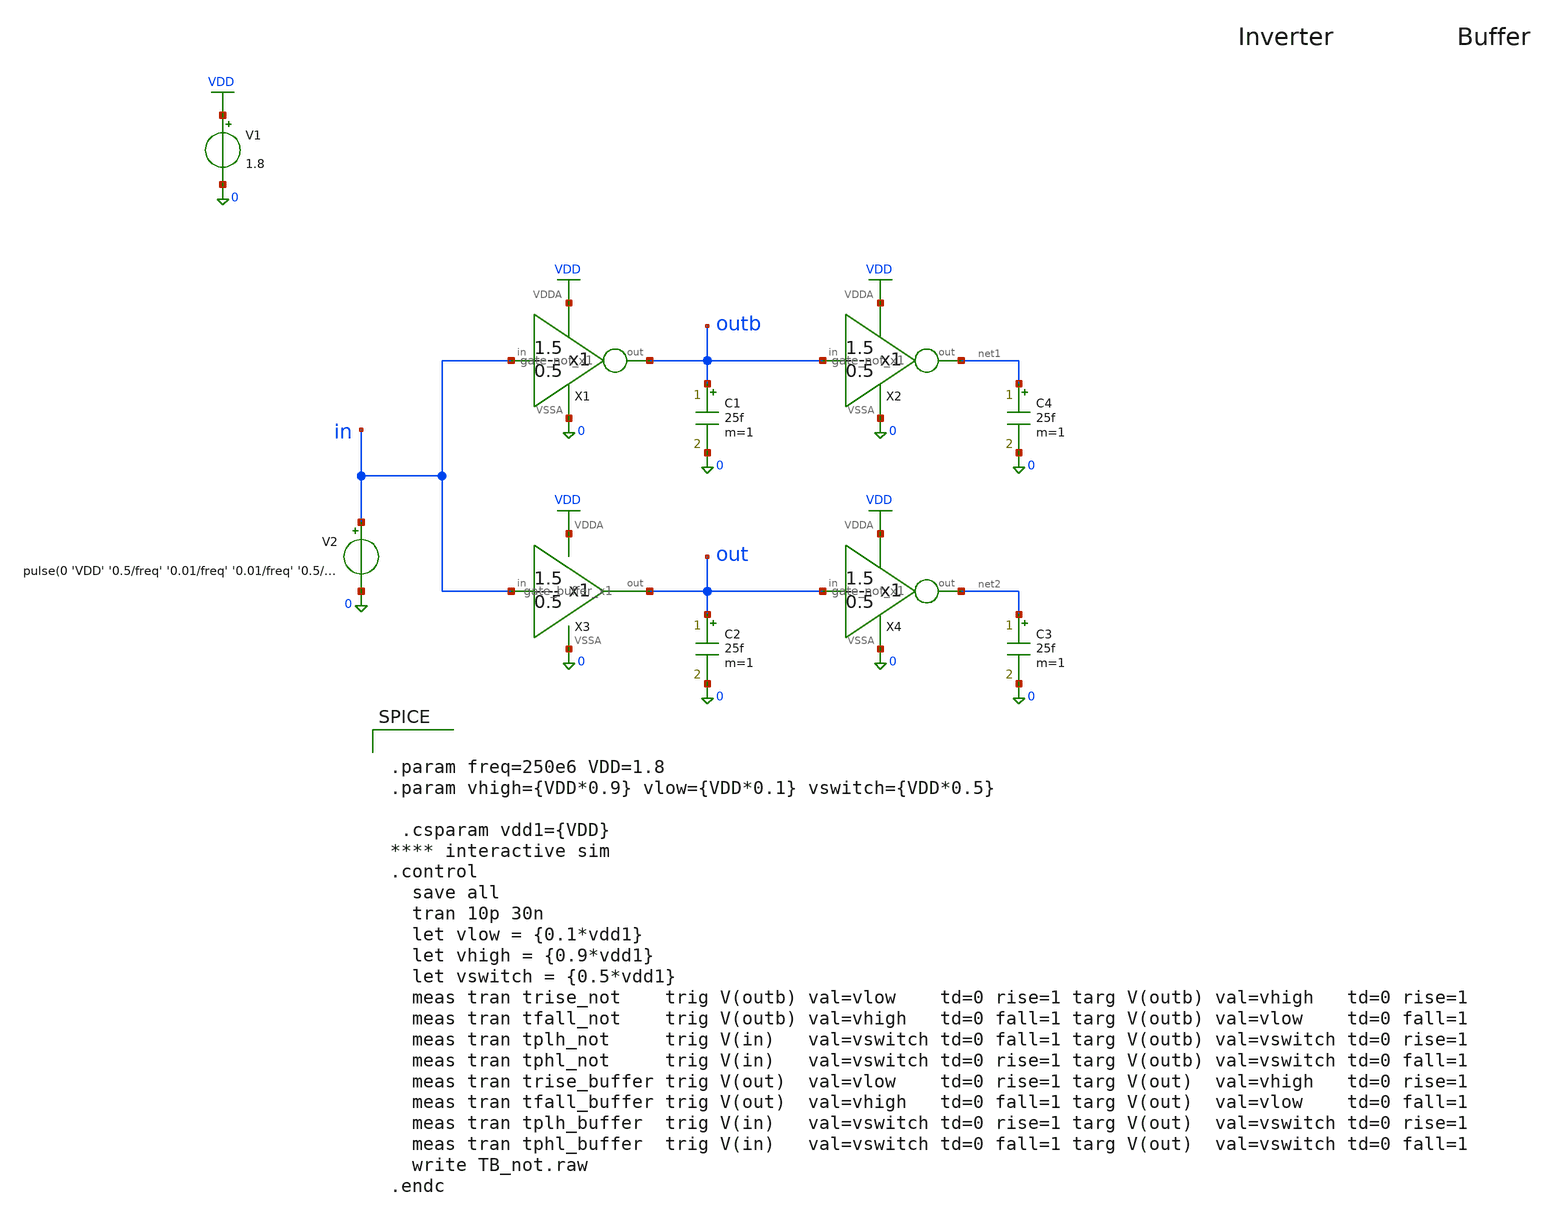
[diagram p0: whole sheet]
** sch_path: sky130A/analog/TB_not.sch
**.subckt TB_not
C1 outb 0 25f m=1
V1 VDD 0 1.8
V2 in 0 pulse(0 'VDD' '0.5/freq' '0.01/freq' '0.01/freq' '0.5/freq' '1/freq')
C4 net1 0 25f m=1
X1 in outb VDD 0 gate_not_x1
X2 outb net1 VDD 0 gate_not_x1
C2 out 0 25f m=1
C3 net2 0 25f m=1
X4 out net2 VDD 0 gate_not_x1
X3 in out VDD 0 gate_buffer_x1
**** begin user architecture code

** opencircuitdesign pdks install
.lib $::SKYWATER_MODELS/sky130.lib.spice tt



.param freq=250e6 VDD=1.8
.param vhigh={VDD*0.9} vlow={VDD*0.1} vswitch={VDD*0.5}

 .csparam vdd1={VDD}
**** interactive sim
.control
  save all
  tran 10p 30n
  let vlow = {0.1*vdd1}
  let vhigh = {0.9*vdd1}
  let vswitch = {0.5*vdd1}
  meas tran trise_not    trig V(outb) val=vlow    td=0 rise=1 targ V(outb) val=vhigh   td=0 rise=1
  meas tran tfall_not    trig V(outb) val=vhigh   td=0 fall=1 targ V(outb) val=vlow    td=0 fall=1
  meas tran tplh_not     trig V(in)   val=vswitch td=0 fall=1 targ V(outb) val=vswitch td=0 rise=1
  meas tran tphl_not     trig V(in)   val=vswitch td=0 rise=1 targ V(outb) val=vswitch td=0 fall=1
  meas tran trise_buffer trig V(out)  val=vlow    td=0 rise=1 targ V(out)  val=vhigh   td=0 rise=1
  meas tran tfall_buffer trig V(out)  val=vhigh   td=0 fall=1 targ V(out)  val=vlow    td=0 fall=1
  meas tran tplh_buffer  trig V(in)   val=vswitch td=0 rise=1 targ V(out)  val=vswitch td=0 rise=1
  meas tran tphl_buffer  trig V(in)   val=vswitch td=0 fall=1 targ V(out)  val=vswitch td=0 fall=1
  write TB_not.raw
.endc


**** end user architecture code
**.ends

* expanding   symbol:  gate_not_x1.sym # of pins=4
** sym_path: sky130A/analog/gate_not_x1.sym
** sch_path: sky130A/analog/gate_not_x1.sch
.subckt gate_not_x1 in out VDDA VSSA
*.ipin in
*.iopin VDDA
*.iopin VSSA
*.opin out
XM1 out in VSSA VSSA sky130_fd_pr__nfet_01v8 L=0.15 W=0.5 nf=1 ad='int((1 + 1)/2) * 0.5 / 1 * 0.29' as='int((1 + 2)/2) * 0.5 / 1 * 0.29'
+ pd='2*int((1 + 1)/2) * (0.5 / 1 + 0.29)' ps='2*int((1 + 2)/2) * (0.5 / 1 + 0.29)' nrd='0.29 / 0.5 ' nrs='0.29 / 0.5 '
+ sa=0 sb=0 sd=0 mult=1 m=1
XM2 out in VDDA VDDA sky130_fd_pr__pfet_01v8 L=0.15 W=1.5 nf=1 ad='int((1 + 1)/2) * 1.5 / 1 * 0.29' as='int((1 + 2)/2) * 1.5 / 1 * 0.29'
+ pd='2*int((1 + 1)/2) * (1.5 / 1 + 0.29)' ps='2*int((1 + 2)/2) * (1.5 / 1 + 0.29)' nrd='0.29 / 1.5 ' nrs='0.29 / 1.5 '
+ sa=0 sb=0 sd=0 mult=1 m=1
.ends


* expanding   symbol:  gate_buffer_x1.sym # of pins=4
** sym_path: sky130A/analog/gate_buffer_x1.sym
** sch_path: sky130A/analog/gate_buffer_x1.sch
.subckt gate_buffer_x1 in out VDDA VSSA
*.ipin in
*.opin out
*.iopin VDDA
*.iopin VSSA
X1 in inb VDDA VSSA gate_not_x1
X2 inb out VDDA VSSA gate_not_x1
.ends

.GLOBAL VDD
.end
